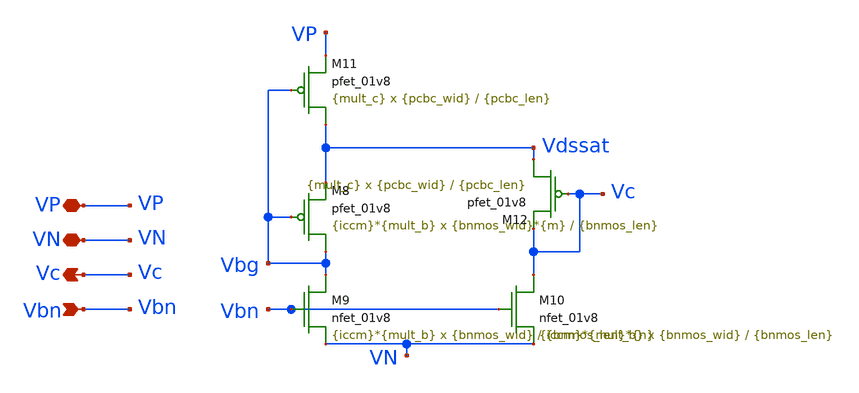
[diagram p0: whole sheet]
** sch_path: cbc.sch
**.subckt cbc VP VN Vc Vbn
*.iopin VP
*.iopin VN
*.opin Vc
*.ipin Vbn
XM8 Vbg Vbg Vdssat VP sky130_fd_pr__pfet_01v8 L={bnmos_len} W={bnmos_wid}*{m} nf=1 ad='int((nf+1)/2) * W/nf * 0.29'
+ as='int((nf+2)/2) * W/nf * 0.29' pd='2*int((nf+1)/2) * (W/nf + 0.29)' ps='2*int((nf+2)/2) * (W/nf + 0.29)'
+ nrd='0.29 / W' nrs='0.29 / W' sa=0 sb=0 sd=0 mult={iccm}*{mult_b} m={iccm}*{mult_b}
XM9 Vbg Vbn VN VN sky130_fd_pr__nfet_01v8 L={bnmos_len}*{n} W={bnmos_wid} nf=1 ad='int((nf+1)/2) * W/nf * 0.29'
+ as='int((nf+2)/2) * W/nf * 0.29' pd='2*int((nf+1)/2) * (W/nf + 0.29)' ps='2*int((nf+2)/2) * (W/nf + 0.29)'
+ nrd='0.29 / W' nrs='0.29 / W' sa=0 sb=0 sd=0 mult={iccm}*{mult_b} m={iccm}*{mult_b}
XM10 Vc Vbn VN VN sky130_fd_pr__nfet_01v8 L={bnmos_len} W={bnmos_wid} nf=1 ad='int((nf+1)/2) * W/nf * 0.29'
+ as='int((nf+2)/2) * W/nf * 0.29' pd='2*int((nf+1)/2) * (W/nf + 0.29)' ps='2*int((nf+2)/2) * (W/nf + 0.29)'
+ nrd='0.29 / W' nrs='0.29 / W' sa=0 sb=0 sd=0 mult={iccm}*{mult_b} m={iccm}*{mult_b}
XM11 Vdssat Vbg VP VP sky130_fd_pr__pfet_01v8 L={pcbc_len} W={pcbc_wid} nf=1 ad='int((nf+1)/2) * W/nf * 0.29'
+ as='int((nf+2)/2) * W/nf * 0.29' pd='2*int((nf+1)/2) * (W/nf + 0.29)' ps='2*int((nf+2)/2) * (W/nf + 0.29)'
+ nrd='0.29 / W' nrs='0.29 / W' sa=0 sb=0 sd=0 mult={mult_c} m={mult_c}
XM12 Vdssat Vc Vc VP sky130_fd_pr__pfet_01v8 L={pcbc_len} W={pcbc_wid} nf=1 ad='int((nf+1)/2) * W/nf * 0.29'
+ as='int((nf+2)/2) * W/nf * 0.29' pd='2*int((nf+1)/2) * (W/nf + 0.29)' ps='2*int((nf+2)/2) * (W/nf + 0.29)'
+ nrd='0.29 / W' nrs='0.29 / W' sa=0 sb=0 sd=0 mult={mult_c} m={mult_c}
**.ends
.end
